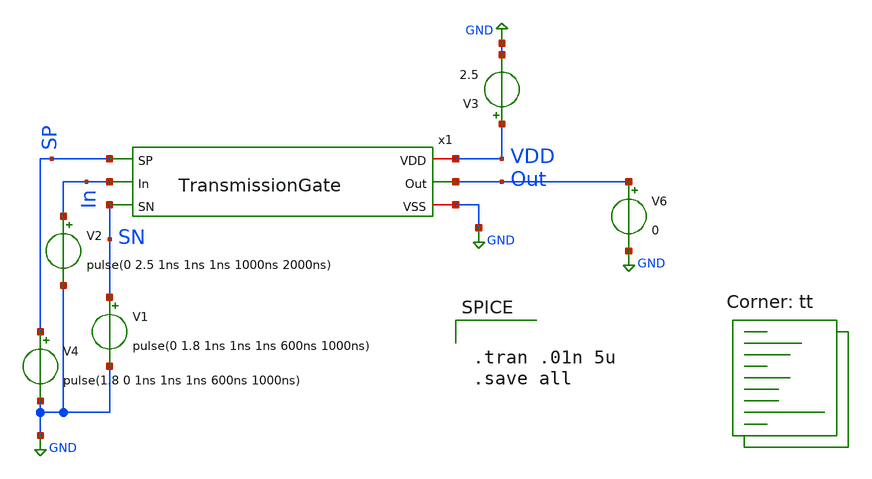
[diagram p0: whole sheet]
** sch_path: xschem/Testbenches/TransmissionGateTB.sch
**.subckt TransmissionGateTB
V2 In GND pulse(0 2.5 1ns 1ns 1ns 1000ns 2000ns)
V1 SN GND pulse(0 1.8 1ns 1ns 1ns 600ns 1000ns)
V3 VDD GND 2.5
V4 SP GND pulse(1.8 0 1ns 1ns 1ns 600ns 1000ns)
x1 SP VDD Out In GND SN TransmissionGate
V6 Out GND 0
**** begin user architecture code
.lib $::SKYWATER_MODELS/sky130.lib.spice tt


.tran .01n 5u
.save all

**** end user architecture code
**.ends

* expanding   symbol:  TransmissionGate.sym # of pins=6
** sym_path: xschem/TransmissionGate.sym
** sch_path: xschem/TransmissionGate.sch
.subckt TransmissionGate SP VDD Out In VSS SN
*.opin Out
*.ipin In
*.ipin SP
*.iopin VDD
*.iopin VSS
*.ipin SN
XM1 In SN Out VSS sky130_fd_pr__nfet_g5v0d10v5 L=0.5 W=0.75 nf=1 ad='int((nf+1)/2) * W/nf * 0.29' as='int((nf+2)/2) * W/nf * 0.29'
+ pd='2*int((nf+1)/2) * (W/nf + 0.29)' ps='2*int((nf+2)/2) * (W/nf + 0.29)' nrd='0.29 / W' nrs='0.29 / W'
+ sa=0 sb=0 sd=0 mult=1 m=1
XM2 In SP Out VDD sky130_fd_pr__pfet_g5v0d10v5 L=0.5 W=1.5 nf=1 ad='int((nf+1)/2) * W/nf * 0.29' as='int((nf+2)/2) * W/nf * 0.29'
+ pd='2*int((nf+1)/2) * (W/nf + 0.29)' ps='2*int((nf+2)/2) * (W/nf + 0.29)' nrd='0.29 / W' nrs='0.29 / W'
+ sa=0 sb=0 sd=0 mult=1 m=1
.ends

.GLOBAL GND
.end
